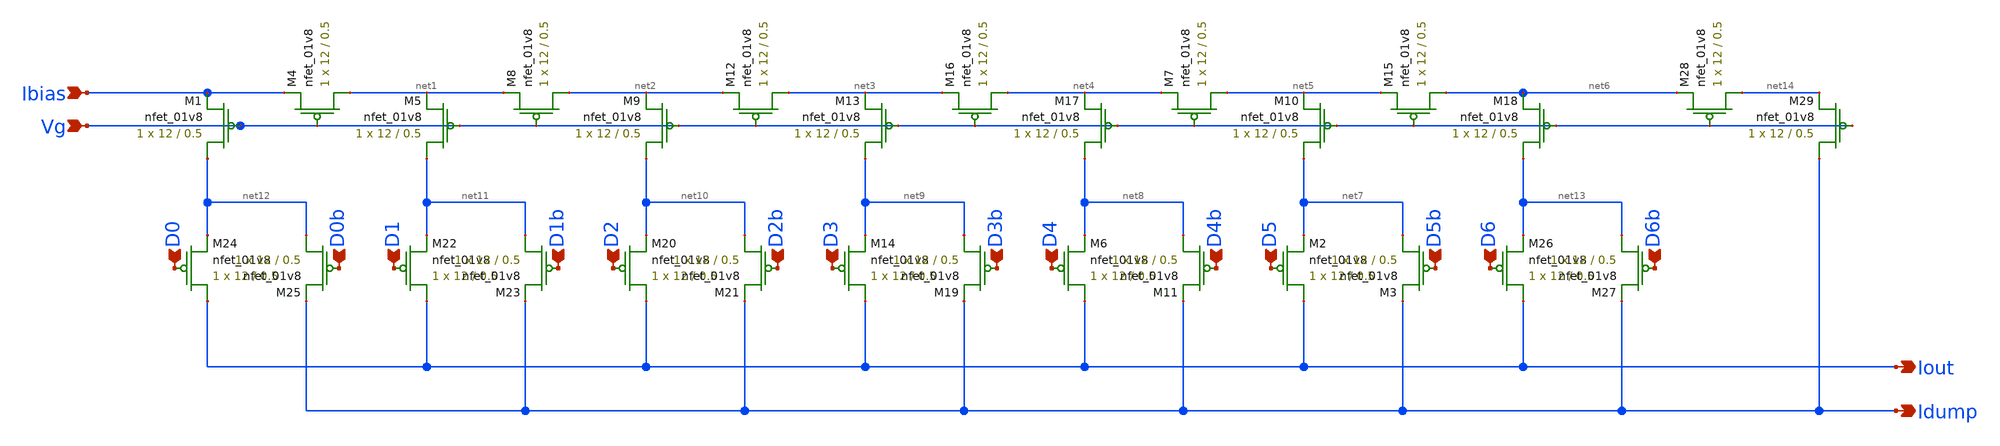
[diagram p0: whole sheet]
** sch_path: schematics/ieee_DAC_pmos.sch
**.subckt ieee_DAC_pmos Ibias Iout D0 D1 D2 D3 D4 D5 D6 Vg D0b D1b D2b D3b D4b D5b D6b Idump
*.ipin Ibias
*.opin Iout
*.ipin D0
*.ipin D1
*.ipin D2
*.ipin D3
*.ipin D4
*.ipin D5
*.ipin D6
*.ipin Vg
*.ipin D0b
*.ipin D1b
*.ipin D2b
*.ipin D3b
*.ipin D4b
*.ipin D5b
*.ipin D6b
*.opin Idump
XM1 net12 Vg Ibias GND sky130_fd_pr__nfet_01v8 L=0.5 W=12 nf=1 ad='int((nf+1)/2) * W/nf * 0.29' as='int((nf+2)/2) * W/nf * 0.29'
+ pd='2*int((nf+1)/2) * (W/nf + 0.29)' ps='2*int((nf+2)/2) * (W/nf + 0.29)' nrd='0.29 / W' nrs='0.29 / W'
+ sa=0 sb=0 sd=0 mult=1 m=1
XM4 net1 Vg Ibias GND sky130_fd_pr__nfet_01v8 L=0.5 W=12 nf=1 ad='int((nf+1)/2) * W/nf * 0.29' as='int((nf+2)/2) * W/nf * 0.29'
+ pd='2*int((nf+1)/2) * (W/nf + 0.29)' ps='2*int((nf+2)/2) * (W/nf + 0.29)' nrd='0.29 / W' nrs='0.29 / W'
+ sa=0 sb=0 sd=0 mult=1 m=1
XM5 net11 Vg net1 GND sky130_fd_pr__nfet_01v8 L=0.5 W=12 nf=1 ad='int((nf+1)/2) * W/nf * 0.29' as='int((nf+2)/2) * W/nf * 0.29'
+ pd='2*int((nf+1)/2) * (W/nf + 0.29)' ps='2*int((nf+2)/2) * (W/nf + 0.29)' nrd='0.29 / W' nrs='0.29 / W'
+ sa=0 sb=0 sd=0 mult=1 m=1
XM8 net2 Vg net1 GND sky130_fd_pr__nfet_01v8 L=0.5 W=12 nf=1 ad='int((nf+1)/2) * W/nf * 0.29' as='int((nf+2)/2) * W/nf * 0.29'
+ pd='2*int((nf+1)/2) * (W/nf + 0.29)' ps='2*int((nf+2)/2) * (W/nf + 0.29)' nrd='0.29 / W' nrs='0.29 / W'
+ sa=0 sb=0 sd=0 mult=1 m=1
XM9 net10 Vg net2 GND sky130_fd_pr__nfet_01v8 L=0.5 W=12 nf=1 ad='int((nf+1)/2) * W/nf * 0.29' as='int((nf+2)/2) * W/nf * 0.29'
+ pd='2*int((nf+1)/2) * (W/nf + 0.29)' ps='2*int((nf+2)/2) * (W/nf + 0.29)' nrd='0.29 / W' nrs='0.29 / W'
+ sa=0 sb=0 sd=0 mult=1 m=1
XM12 net3 Vg net2 GND sky130_fd_pr__nfet_01v8 L=0.5 W=12 nf=1 ad='int((nf+1)/2) * W/nf * 0.29' as='int((nf+2)/2) * W/nf * 0.29'
+ pd='2*int((nf+1)/2) * (W/nf + 0.29)' ps='2*int((nf+2)/2) * (W/nf + 0.29)' nrd='0.29 / W' nrs='0.29 / W'
+ sa=0 sb=0 sd=0 mult=1 m=1
XM13 net9 Vg net3 GND sky130_fd_pr__nfet_01v8 L=0.5 W=12 nf=1 ad='int((nf+1)/2) * W/nf * 0.29' as='int((nf+2)/2) * W/nf * 0.29'
+ pd='2*int((nf+1)/2) * (W/nf + 0.29)' ps='2*int((nf+2)/2) * (W/nf + 0.29)' nrd='0.29 / W' nrs='0.29 / W'
+ sa=0 sb=0 sd=0 mult=1 m=1
XM16 net4 Vg net3 GND sky130_fd_pr__nfet_01v8 L=0.5 W=12 nf=1 ad='int((nf+1)/2) * W/nf * 0.29' as='int((nf+2)/2) * W/nf * 0.29'
+ pd='2*int((nf+1)/2) * (W/nf + 0.29)' ps='2*int((nf+2)/2) * (W/nf + 0.29)' nrd='0.29 / W' nrs='0.29 / W'
+ sa=0 sb=0 sd=0 mult=1 m=1
XM17 net8 Vg net4 GND sky130_fd_pr__nfet_01v8 L=0.5 W=12 nf=1 ad='int((nf+1)/2) * W/nf * 0.29' as='int((nf+2)/2) * W/nf * 0.29'
+ pd='2*int((nf+1)/2) * (W/nf + 0.29)' ps='2*int((nf+2)/2) * (W/nf + 0.29)' nrd='0.29 / W' nrs='0.29 / W'
+ sa=0 sb=0 sd=0 mult=1 m=1
XM7 net5 Vg net4 GND sky130_fd_pr__nfet_01v8 L=0.5 W=12 nf=1 ad='int((nf+1)/2) * W/nf * 0.29' as='int((nf+2)/2) * W/nf * 0.29'
+ pd='2*int((nf+1)/2) * (W/nf + 0.29)' ps='2*int((nf+2)/2) * (W/nf + 0.29)' nrd='0.29 / W' nrs='0.29 / W'
+ sa=0 sb=0 sd=0 mult=1 m=1
XM10 net7 Vg net5 GND sky130_fd_pr__nfet_01v8 L=0.5 W=12 nf=1 ad='int((nf+1)/2) * W/nf * 0.29' as='int((nf+2)/2) * W/nf * 0.29'
+ pd='2*int((nf+1)/2) * (W/nf + 0.29)' ps='2*int((nf+2)/2) * (W/nf + 0.29)' nrd='0.29 / W' nrs='0.29 / W'
+ sa=0 sb=0 sd=0 mult=1 m=1
XM15 net6 Vg net5 GND sky130_fd_pr__nfet_01v8 L=0.5 W=12 nf=1 ad='int((nf+1)/2) * W/nf * 0.29' as='int((nf+2)/2) * W/nf * 0.29'
+ pd='2*int((nf+1)/2) * (W/nf + 0.29)' ps='2*int((nf+2)/2) * (W/nf + 0.29)' nrd='0.29 / W' nrs='0.29 / W'
+ sa=0 sb=0 sd=0 mult=1 m=1
XM18 net13 Vg net6 GND sky130_fd_pr__nfet_01v8 L=0.5 W=12 nf=1 ad='int((nf+1)/2) * W/nf * 0.29' as='int((nf+2)/2) * W/nf * 0.29'
+ pd='2*int((nf+1)/2) * (W/nf + 0.29)' ps='2*int((nf+2)/2) * (W/nf + 0.29)' nrd='0.29 / W' nrs='0.29 / W'
+ sa=0 sb=0 sd=0 mult=1 m=1
XM2 Iout D5 net7 GND sky130_fd_pr__nfet_01v8 L=0.5 W=12 nf=1 ad='int((nf+1)/2) * W/nf * 0.29' as='int((nf+2)/2) * W/nf * 0.29'
+ pd='2*int((nf+1)/2) * (W/nf + 0.29)' ps='2*int((nf+2)/2) * (W/nf + 0.29)' nrd='0.29 / W' nrs='0.29 / W'
+ sa=0 sb=0 sd=0 mult=1 m=1
XM3 net7 D5b Idump GND sky130_fd_pr__nfet_01v8 L=0.5 W=12 nf=1 ad='int((nf+1)/2) * W/nf * 0.29' as='int((nf+2)/2) * W/nf * 0.29'
+ pd='2*int((nf+1)/2) * (W/nf + 0.29)' ps='2*int((nf+2)/2) * (W/nf + 0.29)' nrd='0.29 / W' nrs='0.29 / W'
+ sa=0 sb=0 sd=0 mult=1 m=1
XM6 Iout D4 net8 GND sky130_fd_pr__nfet_01v8 L=0.5 W=12 nf=1 ad='int((nf+1)/2) * W/nf * 0.29' as='int((nf+2)/2) * W/nf * 0.29'
+ pd='2*int((nf+1)/2) * (W/nf + 0.29)' ps='2*int((nf+2)/2) * (W/nf + 0.29)' nrd='0.29 / W' nrs='0.29 / W'
+ sa=0 sb=0 sd=0 mult=1 m=1
XM11 net8 D4b Idump GND sky130_fd_pr__nfet_01v8 L=0.5 W=12 nf=1 ad='int((nf+1)/2) * W/nf * 0.29' as='int((nf+2)/2) * W/nf * 0.29'
+ pd='2*int((nf+1)/2) * (W/nf + 0.29)' ps='2*int((nf+2)/2) * (W/nf + 0.29)' nrd='0.29 / W' nrs='0.29 / W'
+ sa=0 sb=0 sd=0 mult=1 m=1
XM14 Iout D3 net9 GND sky130_fd_pr__nfet_01v8 L=0.5 W=12 nf=1 ad='int((nf+1)/2) * W/nf * 0.29' as='int((nf+2)/2) * W/nf * 0.29'
+ pd='2*int((nf+1)/2) * (W/nf + 0.29)' ps='2*int((nf+2)/2) * (W/nf + 0.29)' nrd='0.29 / W' nrs='0.29 / W'
+ sa=0 sb=0 sd=0 mult=1 m=1
XM19 net9 D3b Idump GND sky130_fd_pr__nfet_01v8 L=0.5 W=12 nf=1 ad='int((nf+1)/2) * W/nf * 0.29' as='int((nf+2)/2) * W/nf * 0.29'
+ pd='2*int((nf+1)/2) * (W/nf + 0.29)' ps='2*int((nf+2)/2) * (W/nf + 0.29)' nrd='0.29 / W' nrs='0.29 / W'
+ sa=0 sb=0 sd=0 mult=1 m=1
XM20 Iout D2 net10 GND sky130_fd_pr__nfet_01v8 L=0.5 W=12 nf=1 ad='int((nf+1)/2) * W/nf * 0.29' as='int((nf+2)/2) * W/nf * 0.29'
+ pd='2*int((nf+1)/2) * (W/nf + 0.29)' ps='2*int((nf+2)/2) * (W/nf + 0.29)' nrd='0.29 / W' nrs='0.29 / W'
+ sa=0 sb=0 sd=0 mult=1 m=1
XM21 net10 D2b Idump GND sky130_fd_pr__nfet_01v8 L=0.5 W=12 nf=1 ad='int((nf+1)/2) * W/nf * 0.29' as='int((nf+2)/2) * W/nf * 0.29'
+ pd='2*int((nf+1)/2) * (W/nf + 0.29)' ps='2*int((nf+2)/2) * (W/nf + 0.29)' nrd='0.29 / W' nrs='0.29 / W'
+ sa=0 sb=0 sd=0 mult=1 m=1
XM22 Iout D1 net11 GND sky130_fd_pr__nfet_01v8 L=0.5 W=12 nf=1 ad='int((nf+1)/2) * W/nf * 0.29' as='int((nf+2)/2) * W/nf * 0.29'
+ pd='2*int((nf+1)/2) * (W/nf + 0.29)' ps='2*int((nf+2)/2) * (W/nf + 0.29)' nrd='0.29 / W' nrs='0.29 / W'
+ sa=0 sb=0 sd=0 mult=1 m=1
XM23 net11 D1b Idump GND sky130_fd_pr__nfet_01v8 L=0.5 W=12 nf=1 ad='int((nf+1)/2) * W/nf * 0.29' as='int((nf+2)/2) * W/nf * 0.29'
+ pd='2*int((nf+1)/2) * (W/nf + 0.29)' ps='2*int((nf+2)/2) * (W/nf + 0.29)' nrd='0.29 / W' nrs='0.29 / W'
+ sa=0 sb=0 sd=0 mult=1 m=1
XM24 Iout D0 net12 GND sky130_fd_pr__nfet_01v8 L=0.5 W=12 nf=1 ad='int((nf+1)/2) * W/nf * 0.29' as='int((nf+2)/2) * W/nf * 0.29'
+ pd='2*int((nf+1)/2) * (W/nf + 0.29)' ps='2*int((nf+2)/2) * (W/nf + 0.29)' nrd='0.29 / W' nrs='0.29 / W'
+ sa=0 sb=0 sd=0 mult=1 m=1
XM25 net12 D0b Idump GND sky130_fd_pr__nfet_01v8 L=0.5 W=12 nf=1 ad='int((nf+1)/2) * W/nf * 0.29' as='int((nf+2)/2) * W/nf * 0.29'
+ pd='2*int((nf+1)/2) * (W/nf + 0.29)' ps='2*int((nf+2)/2) * (W/nf + 0.29)' nrd='0.29 / W' nrs='0.29 / W'
+ sa=0 sb=0 sd=0 mult=1 m=1
XM26 Iout D6 net13 GND sky130_fd_pr__nfet_01v8 L=0.5 W=12 nf=1 ad='int((nf+1)/2) * W/nf * 0.29' as='int((nf+2)/2) * W/nf * 0.29'
+ pd='2*int((nf+1)/2) * (W/nf + 0.29)' ps='2*int((nf+2)/2) * (W/nf + 0.29)' nrd='0.29 / W' nrs='0.29 / W'
+ sa=0 sb=0 sd=0 mult=1 m=1
XM27 net13 D6b Idump GND sky130_fd_pr__nfet_01v8 L=0.5 W=12 nf=1 ad='int((nf+1)/2) * W/nf * 0.29' as='int((nf+2)/2) * W/nf * 0.29'
+ pd='2*int((nf+1)/2) * (W/nf + 0.29)' ps='2*int((nf+2)/2) * (W/nf + 0.29)' nrd='0.29 / W' nrs='0.29 / W'
+ sa=0 sb=0 sd=0 mult=1 m=1
XM28 net14 Vg net6 GND sky130_fd_pr__nfet_01v8 L=0.5 W=12 nf=1 ad='int((nf+1)/2) * W/nf * 0.29' as='int((nf+2)/2) * W/nf * 0.29'
+ pd='2*int((nf+1)/2) * (W/nf + 0.29)' ps='2*int((nf+2)/2) * (W/nf + 0.29)' nrd='0.29 / W' nrs='0.29 / W'
+ sa=0 sb=0 sd=0 mult=1 m=1
XM29 Idump Vg net14 GND sky130_fd_pr__nfet_01v8 L=0.5 W=12 nf=1 ad='int((nf+1)/2) * W/nf * 0.29' as='int((nf+2)/2) * W/nf * 0.29'
+ pd='2*int((nf+1)/2) * (W/nf + 0.29)' ps='2*int((nf+2)/2) * (W/nf + 0.29)' nrd='0.29 / W' nrs='0.29 / W'
+ sa=0 sb=0 sd=0 mult=1 m=1
**.ends
.end
